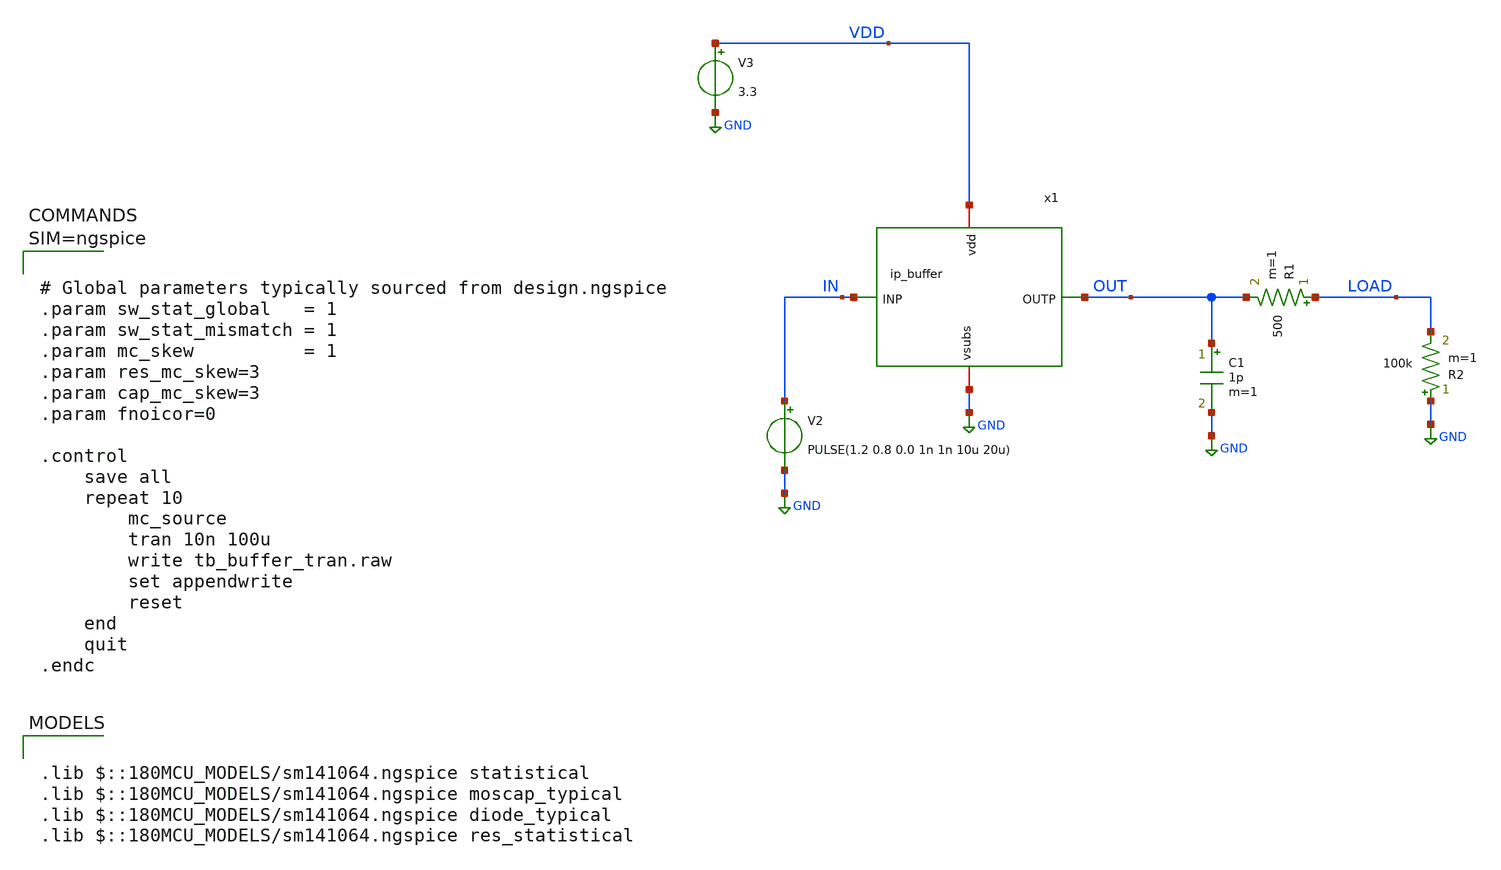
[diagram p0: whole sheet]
** sch_path: xschem/tb_buffer_tran.sch
**.subckt tb_buffer_tran
x1 VDD OUT IN GND ip_buffer
V3 VDD GND 3.3
R1 LOAD OUT 500 m=1
C1 OUT GND 1p m=1
R2 GND LOAD 100k m=1
V2 IN GND PULSE(1.2 0.8 0.0 1n 1n 10u 20u)
**** begin user architecture code

.lib $::180MCU_MODELS/sm141064.ngspice statistical
.lib $::180MCU_MODELS/sm141064.ngspice moscap_typical
.lib $::180MCU_MODELS/sm141064.ngspice diode_typical
.lib $::180MCU_MODELS/sm141064.ngspice res_statistical




# Global parameters typically sourced from design.ngspice
.param sw_stat_global   = 1
.param sw_stat_mismatch = 1
.param mc_skew          = 1
.param res_mc_skew=3
.param cap_mc_skew=3
.param fnoicor=0

.control
	save all
	repeat 10
		mc_source
		tran 10n 100u
		write tb_buffer_tran.raw
		set appendwrite
		reset
	end
	quit
.endc



**** end user architecture code
**.ends

* expanding   symbol:  ip_buffer.sym # of pins=4
** sym_path: xschem/ip_buffer.sym
** sch_path: xschem/ip_buffer.sch
.subckt ip_buffer vdd OUTP INP vsubs
*.iopin vsubs
*.iopin vdd
*.ipin INP
*.opin OUTP
XM1 vsubs INP OUTP OUTP pfet_06v0 L=1u W=10u nf=1 ad='int((nf+1)/2) * W/nf * 0.18u' as='int((nf+2)/2) * W/nf * 0.18u'
+ pd='2*int((nf+1)/2) * (W/nf + 0.18u)' ps='2*int((nf+2)/2) * (W/nf + 0.18u)' nrd='0.18u / W' nrs='0.18u / W'
+ sa=0 sb=0 sd=0 m=15
R1 net2 vsubs 36k m=1
Vmeas net1 net2 0
XM4 OUTP net1 vdd vdd pfet_06v0 L=2u W=10u nf=1 ad='int((nf+1)/2) * W/nf * 0.18u' as='int((nf+2)/2) * W/nf * 0.18u'
+ pd='2*int((nf+1)/2) * (W/nf + 0.18u)' ps='2*int((nf+2)/2) * (W/nf + 0.18u)' nrd='0.18u / W' nrs='0.18u / W'
+ sa=0 sb=0 sd=0 m=5
XM2 net1 net1 vdd vdd pfet_06v0 L=2u W=10u nf=1 ad='int((nf+1)/2) * W/nf * 0.18u' as='int((nf+2)/2) * W/nf * 0.18u'
+ pd='2*int((nf+1)/2) * (W/nf + 0.18u)' ps='2*int((nf+2)/2) * (W/nf + 0.18u)' nrd='0.18u / W' nrs='0.18u / W'
+ sa=0 sb=0 sd=0 m=3
.ends

.GLOBAL GND
.end
